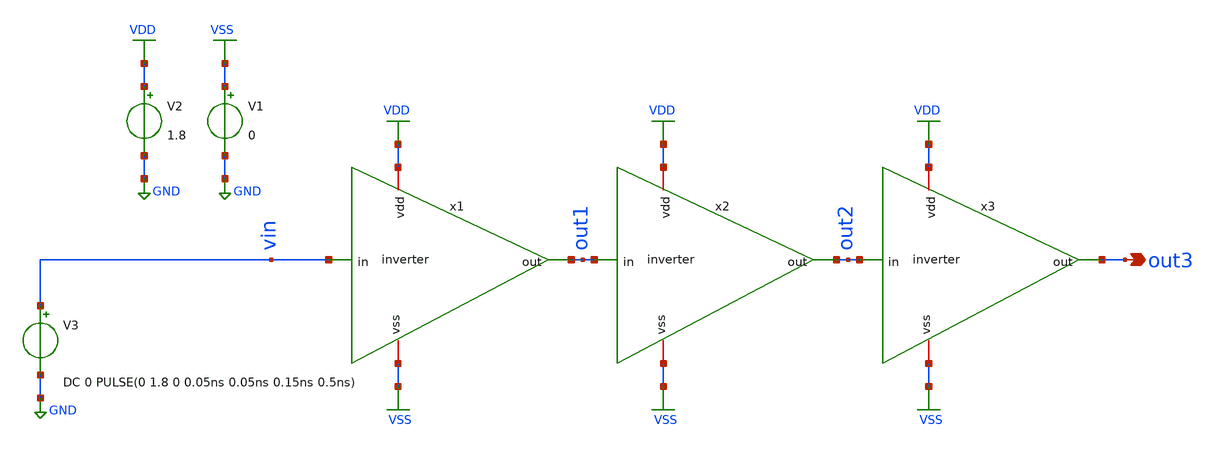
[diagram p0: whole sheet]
** sch_path: scripts/inverter-chain/tb_realistic_source.sch
**.subckt tb_realistic_source out3
*.opin out3
V1 VSS GND 0
V2 VDD GND 1.8
V3 vin GND

DC 0 PULSE(0 1.8 0 0.05ns 0.05ns 0.15ns 0.5ns)


x1 VDD out1 vin VSS inverter
x2 VDD out2 out1 VSS inverter
x3 VDD out3 out2 VSS inverter
**** begin user architecture code



.param pp = 3.27
.param pn = 0.42

********************************
* Control section
********************************
.control

* Voltage values to calculate rise and fall times
let v_steady = 1.8
let per10 = v_steady * 0.1
let per90 = v_steady * 0.9
let per50 = v_steady * 0.5

* These limits are based on the design of a standard cell of 12 tracks.
let wp_max = 1.85
let wn_min = 0.41
let wp_min = 0.42
let wn_max = 1.84

* Initialization of variables and size of iteration.
let delta_w = 0.005
let wp = wp_max
let wn = wn_min
let loop = 0

* These vector will be used to save the data of each iteration.
let loops = (wp_max-wn_min)/delta_w
let wpv = unitvec($&loops)
let wnv = unitvec($&loops)
let trv = unitvec($&loops)
let tfv = unitvec($&loops)

* Start loop
while wp ge wp_min

* Modify widths
  echo
  echo ********************************** Cycle $&loop **********************************
  echo
  alterparam pp = $&wp
  reset
  alterparam pn = $&wn
  reset

* Run transient analysis
  TRAN 0.01n 1.5n $ 3 periods

* Find rise and fall times
  echo
  meas  TRAN  t_rise  TRIG  v(out2) VAL=per10 RISE=2  TARG v(out2)  VAL=per90 RISE=2
  meas  TRAN  t_fall  TRIG  v(out2) VAL=per90 FALL=2  TARG v(out2)  VAL=per10 FALL=2
  echo Wn: $&wn
  echo Wp: $&wp
  echo

* Save widths, t_rise, t_fall in vectors
  let wnv[loop] = wn
  let wpv[loop] = wp
  let trv[loop] = t_rise
  let tfv[loop] = t_fall

* Modify widths
  let wn = wn + delta_w
  let wp = wp - delta_w

* Counter increment
  let loop = loop + 1

end

echo
echo ********************************** End of Simulation **********************************
echo

* Export vector data into raw file
write data_rvs_VACIO.raw wnv wpv trv tfv

* Plot both rise and fall times vs. NMOS widths
* plot trv vs wnv, tfv vs wnv
.endc






.lib $::SKYWATER_MODELS/sky130.lib.spice VACIO

.param mc_mm_switch=0
.param mc_pr_switch=1


**** end user architecture code
**.ends
.GLOBAL VSS
.GLOBAL VDD
.GLOBAL GND
.end
